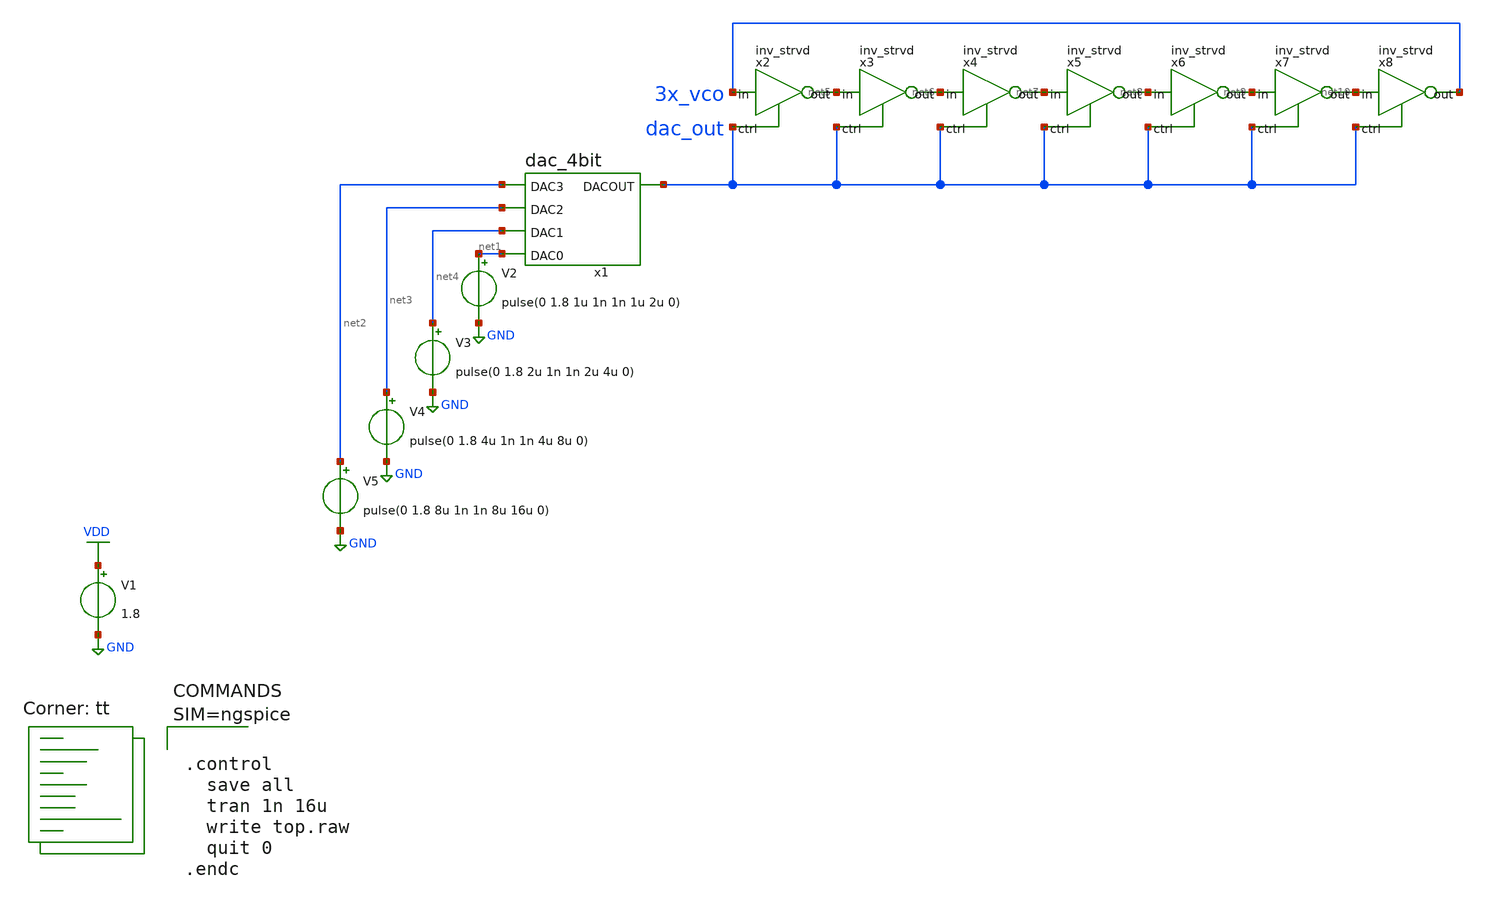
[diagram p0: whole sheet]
** sch_path: tt_um_wulf_8bit_vco/xschem/top_4bit.sch
**.subckt top_4bit
x1 dac_out net2 net3 net4 net1 VDD GND dac_4bit
V1 VDD GND 1.8
V2 net1 GND pulse(0 1.8 1u 1n 1n 1u 2u 0)
V3 net4 GND pulse(0 1.8 2u 1n 1n 2u 4u 0)
V4 net3 GND pulse(0 1.8 4u 1n 1n 4u 8u 0)
V5 net2 GND pulse(0 1.8 8u 1n 1n 8u 16u 0)
x2 3x_vco net5 dac_out VDD GND inv_strvd
x3 net5 net6 dac_out VDD GND inv_strvd
x4 net6 net7 dac_out VDD GND inv_strvd
x5 net7 net8 dac_out VDD GND inv_strvd
x6 net8 net9 dac_out VDD GND inv_strvd
x7 net9 net10 dac_out VDD GND inv_strvd
x8 net10 3x_vco dac_out VDD GND inv_strvd
**** begin user architecture code



.control
  save all
  tran 1n 16u
  write top.raw
  quit 0
.endc



.lib $::SKYWATER_MODELS/sky130.lib.spice tt



.include ~/design/lib/inv_small.spice



**** end user architecture code
**.ends
.GLOBAL GND
.GLOBAL VDD
.end
